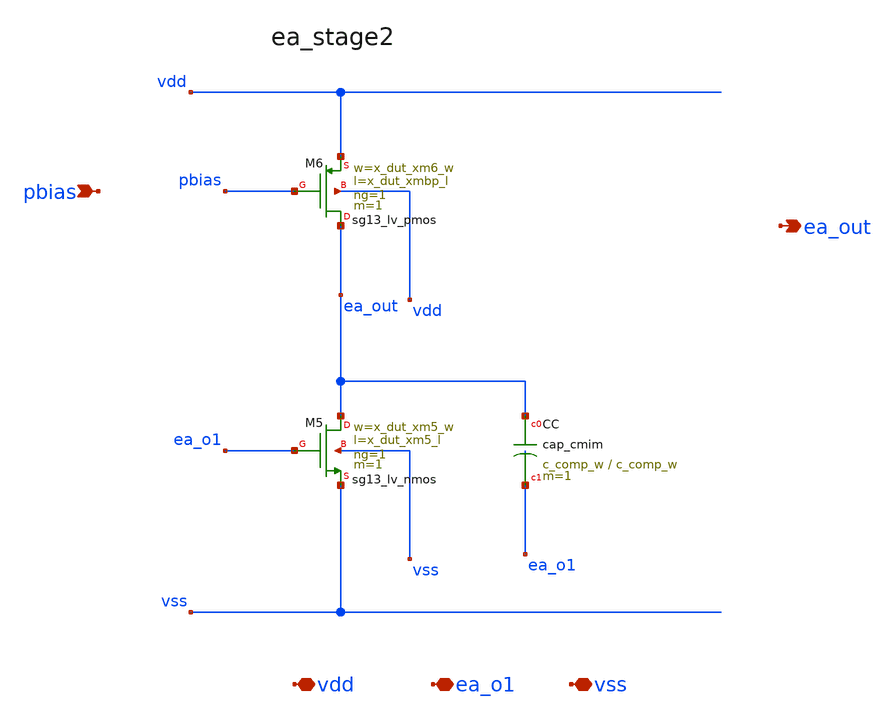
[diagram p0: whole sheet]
** sch_path: analog-db/circuits/ldo_010_capless_lowiq/pdk/ihp-sg13g2/schematic/blocks/ea_stage2.sch
**.subckt ea_stage2 pbias vdd ea_o1 vss ea_out
*.ipin pbias
*.iopin vdd
*.iopin ea_o1
*.iopin vss
*.opin ea_out
XM5 ea_out ea_o1 vss vss sg13_lv_nmos w=x_dut_xm5_w l=x_dut_xm5_l ng=1 m=1 mm_ok=1
XM6 ea_out pbias vdd vdd sg13_lv_pmos w=x_dut_xm6_w l=x_dut_xmbp_l ng=1 m=1 mm_ok=1
XCC ea_out ea_o1 cap_cmim w=c_comp_w l=c_comp_w m=1
**.ends
.end
